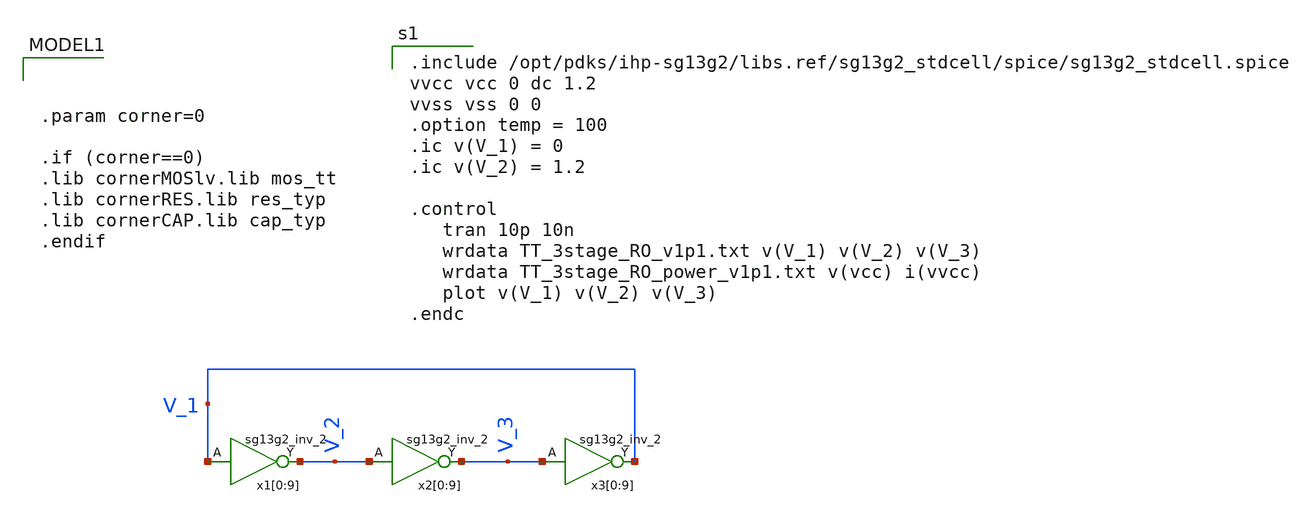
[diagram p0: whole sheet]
** sch_path: Day1/tb_3stage_RO.sch
* IHP-GmbH/IHP-Open-PDK/ihp-sg13g2/libs.tech/xschem/sg13g2_stdcells/sg13g2_inv_2.sch:
* Copyright 2023 IHP PDK Authors
* Licensed under the Apache License, Version 2.0 (the "License");
**.subckt tb_3stage_RO
x1[0] V_2 V_1 VCC VSS sg13g2_inv_2
x1[1] V_2 V_1 VCC VSS sg13g2_inv_2
x1[2] V_2 V_1 VCC VSS sg13g2_inv_2
x1[3] V_2 V_1 VCC VSS sg13g2_inv_2
x1[4] V_2 V_1 VCC VSS sg13g2_inv_2
x1[5] V_2 V_1 VCC VSS sg13g2_inv_2
x1[6] V_2 V_1 VCC VSS sg13g2_inv_2
x1[7] V_2 V_1 VCC VSS sg13g2_inv_2
x1[8] V_2 V_1 VCC VSS sg13g2_inv_2
x1[9] V_2 V_1 VCC VSS sg13g2_inv_2
x2[0] V_3 V_2 VCC VSS sg13g2_inv_2
x2[1] V_3 V_2 VCC VSS sg13g2_inv_2
x2[2] V_3 V_2 VCC VSS sg13g2_inv_2
x2[3] V_3 V_2 VCC VSS sg13g2_inv_2
x2[4] V_3 V_2 VCC VSS sg13g2_inv_2
x2[5] V_3 V_2 VCC VSS sg13g2_inv_2
x2[6] V_3 V_2 VCC VSS sg13g2_inv_2
x2[7] V_3 V_2 VCC VSS sg13g2_inv_2
x2[8] V_3 V_2 VCC VSS sg13g2_inv_2
x2[9] V_3 V_2 VCC VSS sg13g2_inv_2
x3[0] V_1 V_3 VCC VSS sg13g2_inv_2
x3[1] V_1 V_3 VCC VSS sg13g2_inv_2
x3[2] V_1 V_3 VCC VSS sg13g2_inv_2
x3[3] V_1 V_3 VCC VSS sg13g2_inv_2
x3[4] V_1 V_3 VCC VSS sg13g2_inv_2
x3[5] V_1 V_3 VCC VSS sg13g2_inv_2
x3[6] V_1 V_3 VCC VSS sg13g2_inv_2
x3[7] V_1 V_3 VCC VSS sg13g2_inv_2
x3[8] V_1 V_3 VCC VSS sg13g2_inv_2
x3[9] V_1 V_3 VCC VSS sg13g2_inv_2
**** begin user architecture code

.include /opt/pdks/ihp-sg13g2/libs.ref/sg13g2_stdcell/spice/sg13g2_stdcell.spice
vvcc vcc 0 dc 1.2
vvss vss 0 0
.option temp = 100
.ic v(V_1) = 0
.ic v(V_2) = 1.2

.control
   tran 10p 10n
   wrdata TT_3stage_RO_v1p1.txt v(V_1) v(V_2) v(V_3)
   wrdata TT_3stage_RO_power_v1p1.txt v(vcc) i(vvcc)
   plot v(V_1) v(V_2) v(V_3)
.endc




.param corner=0

.if (corner==0)
.lib cornerMOSlv.lib mos_tt
.lib cornerRES.lib res_typ
.lib cornerCAP.lib cap_typ
.endif

**** end user architecture code
**.ends

* expanding   symbol:  sg13g2_inv_2.sym # of pins=2
** sym_path: sg13g2_inv_2.sym
** sch_path: sg13g2_inv_2.sch
.subckt sg13g2_inv_2 Y A VDD VSS
*.opin Y
*.ipin A
*.iopin VDD
*.iopin VSS
XM1 Y A VSS VSS sg13_lv_nmos w=1.48u l=130.00n ng=2 m=1 mm_ok=1
XM2 Y A VDD VDD sg13_lv_pmos w=2.24u l=130.00n ng=2 m=1 mm_ok=1
.ends

.end
